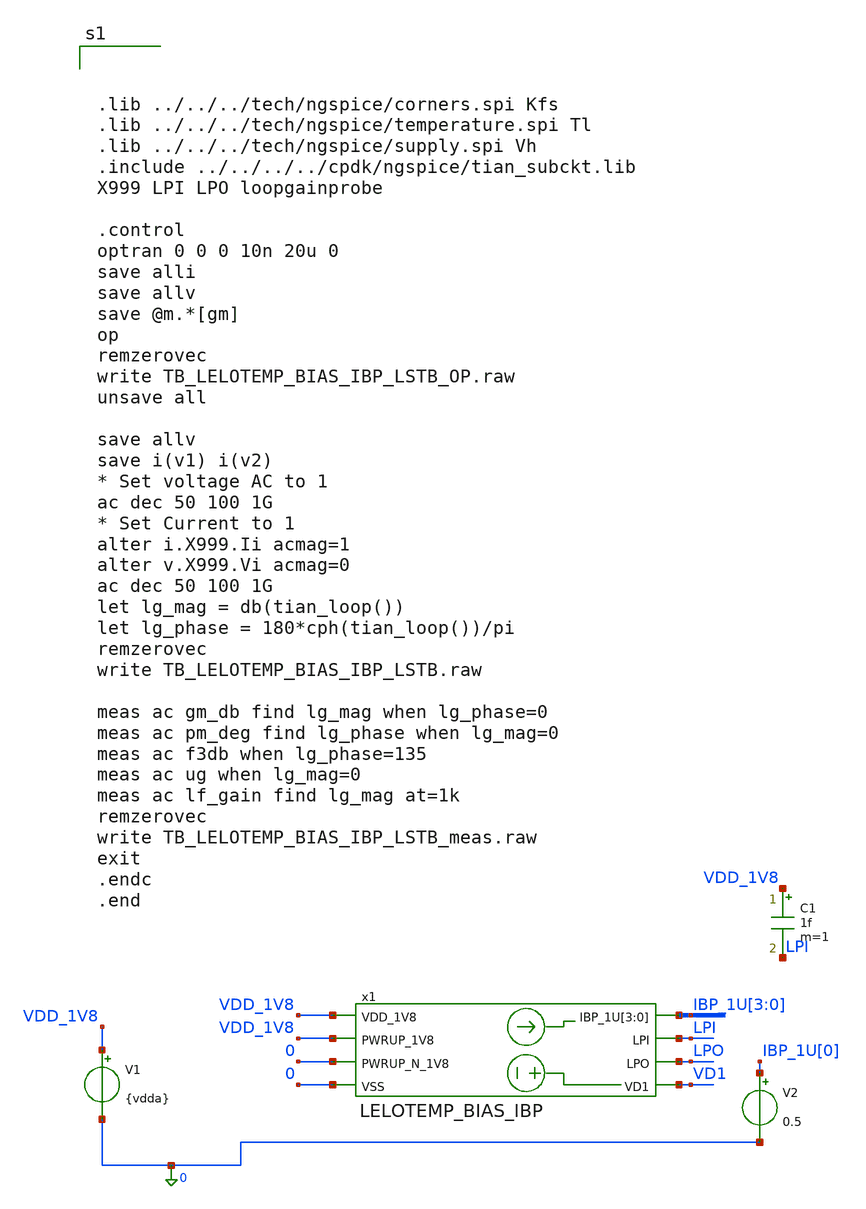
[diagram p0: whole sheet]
** sch_path: design/LELO_TEMP_SKY130A/TB_LELOTEMP_BIAS_IBP_LSTB.sch
**.subckt TB_LELOTEMP_BIAS_IBP_LSTB
V1 VDD_1V8 0 {vdda}
V2 IBP_1U[0] 0 0.5
x1 VDD_1V8 LPI IBP_1U[3] IBP_1U[2] IBP_1U[1] IBP_1U[0] LPO VD1 VDD_1V8 0 0 LELOTEMP_BIAS_IBP
C1 VDD_1V8 LPI 1f m=1
**** begin user architecture code



.lib ../../../tech/ngspice/corners.spi Kfs
.lib ../../../tech/ngspice/temperature.spi Tl
.lib ../../../tech/ngspice/supply.spi Vh
.include ../../../../cpdk/ngspice/tian_subckt.lib
X999 LPI LPO loopgainprobe

.control
optran 0 0 0 10n 20u 0
save alli
save allv
save @m.*[gm]
op
remzerovec
write TB_LELOTEMP_BIAS_IBP_LSTB_OP.raw
unsave all

save allv
save i(v1) i(v2)
* Set voltage AC to 1
ac dec 50 100 1G
* Set Current to 1
alter i.X999.Ii acmag=1
alter v.X999.Vi acmag=0
ac dec 50 100 1G
let lg_mag = db(tian_loop())
let lg_phase = 180*cph(tian_loop())/pi
remzerovec
write TB_LELOTEMP_BIAS_IBP_LSTB.raw

meas ac gm_db find lg_mag when lg_phase=0
meas ac pm_deg find lg_phase when lg_mag=0
meas ac f3db when lg_phase=135
meas ac ug when lg_mag=0
meas ac lf_gain find lg_mag at=1k
remzerovec
write TB_LELOTEMP_BIAS_IBP_LSTB_meas.raw
exit
.endc
.end



**** end user architecture code
**.ends
.end
